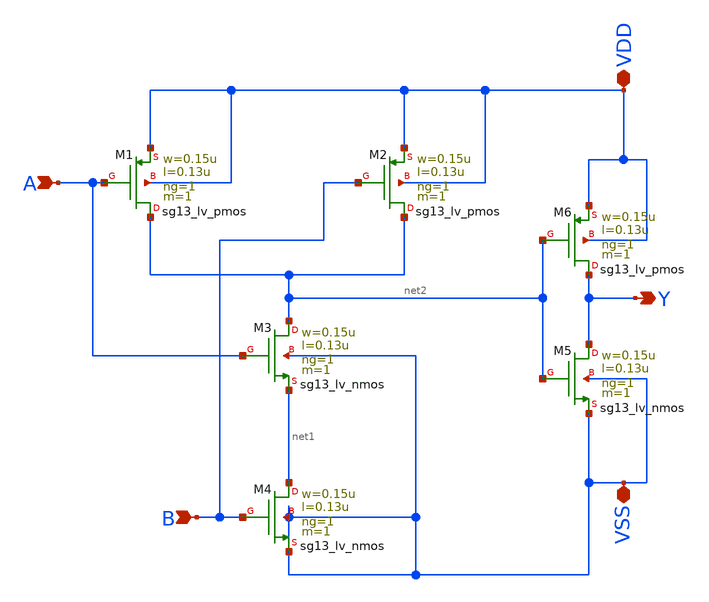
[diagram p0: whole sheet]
** sch_path: AND2.sch
**.subckt AND2 A B Y VDD VSS
*.ipin A
*.ipin B
*.opin Y
*.iopin VDD
*.iopin VSS
XM2 net2 B VDD VDD sg13_lv_pmos w=0.15u l=0.13u ng=1 m=1 mm_ok=1
XM1 net2 A VDD VDD sg13_lv_pmos w=0.15u l=0.13u ng=1 m=1 mm_ok=1
XM3 net2 A net1 VSS sg13_lv_nmos w=0.15u l=0.13u ng=1 m=1 mm_ok=1
XM4 net1 B VSS VSS sg13_lv_nmos w=0.15u l=0.13u ng=1 m=1 mm_ok=1
XM5 Y net2 VSS VSS sg13_lv_nmos w=0.15u l=0.13u ng=1 m=1 mm_ok=1
XM6 Y net2 VDD VDD sg13_lv_pmos w=0.15u l=0.13u ng=1 m=1 mm_ok=1
**.ends
.end
